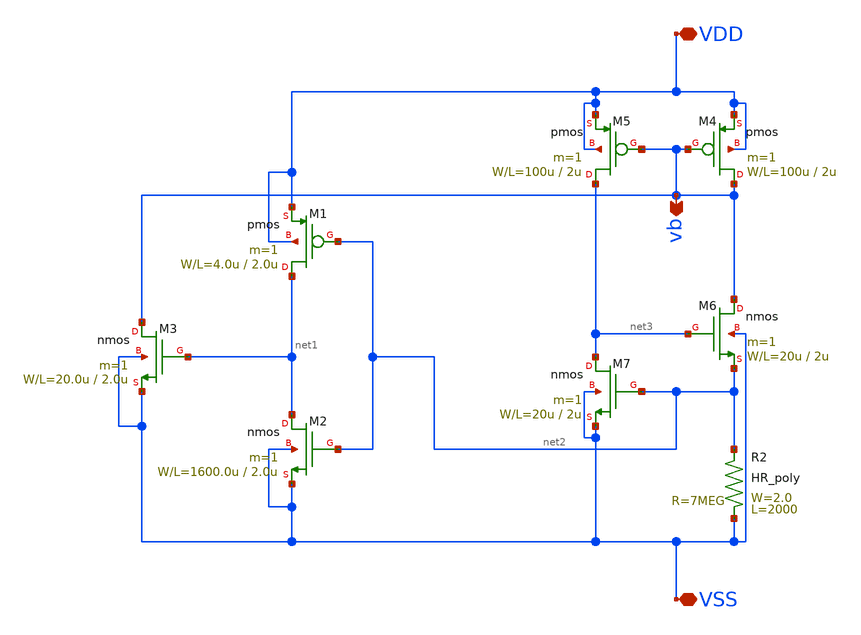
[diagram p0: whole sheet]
** sch_path: OR1/PTC06/current-source/cs_startup_usage.sch
**.subckt cs_startup_usage VDD VSS vb
*.iopin VDD
*.iopin VSS
*.opin vb
M1 net1 net2 VDD VDD pmos L=2.0u W=4.0u m=1
M2 net1 net2 VSS VSS nmos L=2.0u W=1600.0u m=1
M3 vb net1 VSS VSS nmos L=2.0u W=20.0u m=1
R2 VSS net2 HR_poly W=2.0 L=2000
M4 vb vb VDD VDD pmos L=2u W=100u m=1
M5 net3 vb VDD VDD pmos L=2u W=100u m=1
M6 vb net3 net2 VSS nmos L=2u W=20u m=1
M7 net3 net2 VSS VSS nmos L=2u W=20u m=1
**.ends
.end
